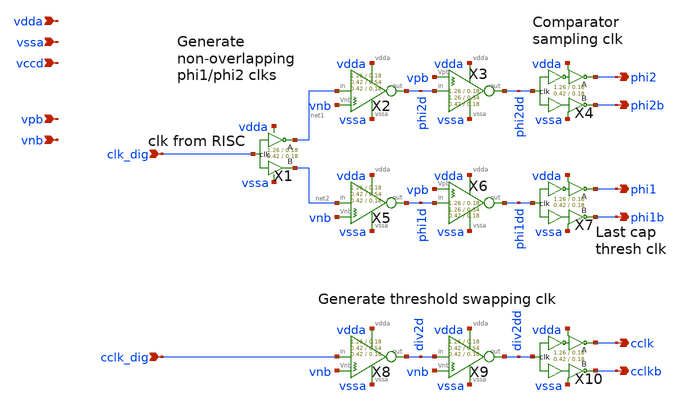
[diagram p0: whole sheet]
** sch_path: xschem/clkgen/filter_clkgen.sch
**.subckt filter_clkgen clk_dig phi2 phi2b phi1 phi1b cclk cclkb vpb vnb vdda vssa cclk_dig vccd
*.ipin clk_dig
*.opin phi2
*.opin phi2b
*.opin phi1
*.opin phi1b
*.opin cclk
*.opin cclkb
*.ipin vpb
*.ipin vnb
*.ipin vdda
*.ipin vssa
*.ipin cclk_dig
*.ipin vccd
X4 phi2dd phi2 phi2b vdda vssa comp_clks Wpmos=1.26 Lpmos=0.18 Wnmos=0.42 Lnmos=0.18
X7 phi1dd phi1 phi1b vdda vssa comp_clks Wpmos=1.26 Lpmos=0.18 Wnmos=0.42 Lnmos=0.18
X10 div2dd cclk cclkb vdda vssa comp_clks Wpmos=1.26 Lpmos=0.18 Wnmos=0.42 Lnmos=0.18
X1 clk_dig net1 net2 vdda vssa comp_clks_1stage Wpmos=1.26 Lpmos=0.18 Wnmos=0.42 Lnmos=0.18
X2 net1 phi2d vnb vdda vssa inv_weak_pulldown Wpmos=1.26 Lpmos= Wnmos= Lnmos=0.54
X5 net2 phi1d vnb vdda vssa inv_weak_pulldown Wpmos=1.26 Lpmos= Wnmos= Lnmos=0.54
X8 cclk_dig div2d vnb vdda vssa inv_weak_pulldown Wpmos=1.26 Lpmos= Wnmos= Lnmos=0.54
X9 div2d div2dd vnb vdda vssa inv_weak_pulldown Wpmos=1.26 Lpmos= Wnmos= Lnmos=0.54
X3 phi2d phi2dd vpb vdda vssa inv_weak_pullup Wpmos=1.26 Lpmos=0.54 Wnmos= Lnmos=
X6 phi1d phi1dd vpb vdda vssa inv_weak_pullup Wpmos=1.26 Lpmos=0.54 Wnmos= Lnmos=
**.ends
.end
